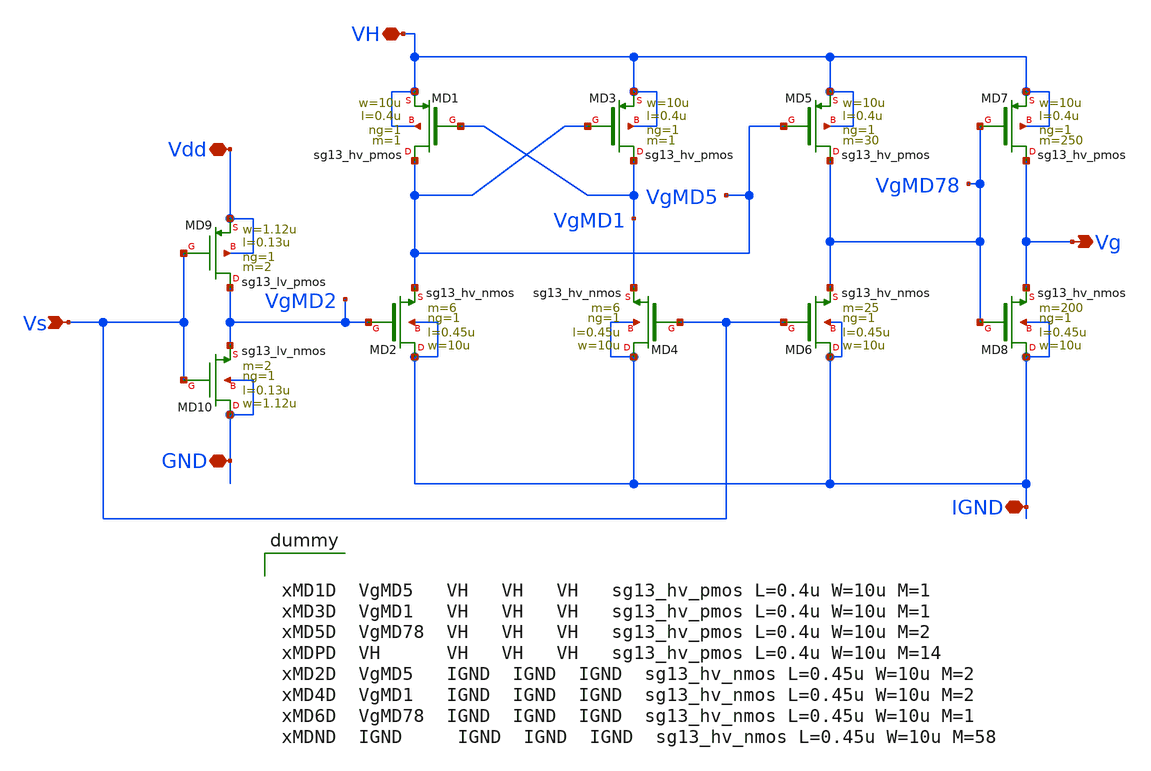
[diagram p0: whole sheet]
** sch_path: ChipUSM_AnalogTrack24/GD/GD_vto1p1.sch
**.subckt GD_vto1p1 VH Vdd Vs Vg GND IGND
*.iopin VH
*.iopin Vdd
*.ipin Vs
*.opin Vg
*.iopin GND
*.iopin IGND
XMD9 VgMD2 Vs Vdd Vdd sg13_lv_pmos w=1.12u l=0.13u ng=1 m=2 mm_ok=1
XMD10 GND Vs VgMD2 GND sg13_lv_nmos w=1.12u l=0.13u ng=1 m=2 mm_ok=1
XMD1 VgMD5 VgMD1 VH VH sg13_hv_pmos w=10u l=0.4u ng=1 m=1 mm_ok=1
XMD3 VgMD1 VgMD5 VH VH sg13_hv_pmos w=10u l=0.4u ng=1 m=1 mm_ok=1
XMD5 VgMD78 VgMD5 VH VH sg13_hv_pmos w=10u l=0.4u ng=1 m=30 mm_ok=1
XMD7 Vg VgMD78 VH VH sg13_hv_pmos w=10u l=0.4u ng=1 m=250 mm_ok=1
XMD2 IGND VgMD2 VgMD5 IGND sg13_hv_nmos w=10u l=0.45u ng=1 m=6 mm_ok=1
XMD4 IGND Vs VgMD1 IGND sg13_hv_nmos w=10u l=0.45u ng=1 m=6 mm_ok=1
XMD6 IGND Vs VgMD78 IGND sg13_hv_nmos w=10u l=0.45u ng=1 m=25 mm_ok=1
XMD8 IGND VgMD78 Vg IGND sg13_hv_nmos w=10u l=0.45u ng=1 m=200 mm_ok=1
**** begin user architecture code


xMD1D  VgMD5   VH   VH   VH   sg13_hv_pmos L=0.4u W=10u M=1
xMD3D  VgMD1   VH   VH   VH   sg13_hv_pmos L=0.4u W=10u M=1
xMD5D  VgMD78  VH   VH   VH   sg13_hv_pmos L=0.4u W=10u M=2
xMDPD  VH      VH   VH   VH   sg13_hv_pmos L=0.4u W=10u M=14
xMD2D  VgMD5   IGND  IGND  IGND  sg13_hv_nmos L=0.45u W=10u M=2
xMD4D  VgMD1   IGND  IGND  IGND  sg13_hv_nmos L=0.45u W=10u M=2
xMD6D  VgMD78  IGND  IGND  IGND  sg13_hv_nmos L=0.45u W=10u M=1
xMDND  IGND     IGND  IGND  IGND  sg13_hv_nmos L=0.45u W=10u M=58


**** end user architecture code
**.ends
.end
